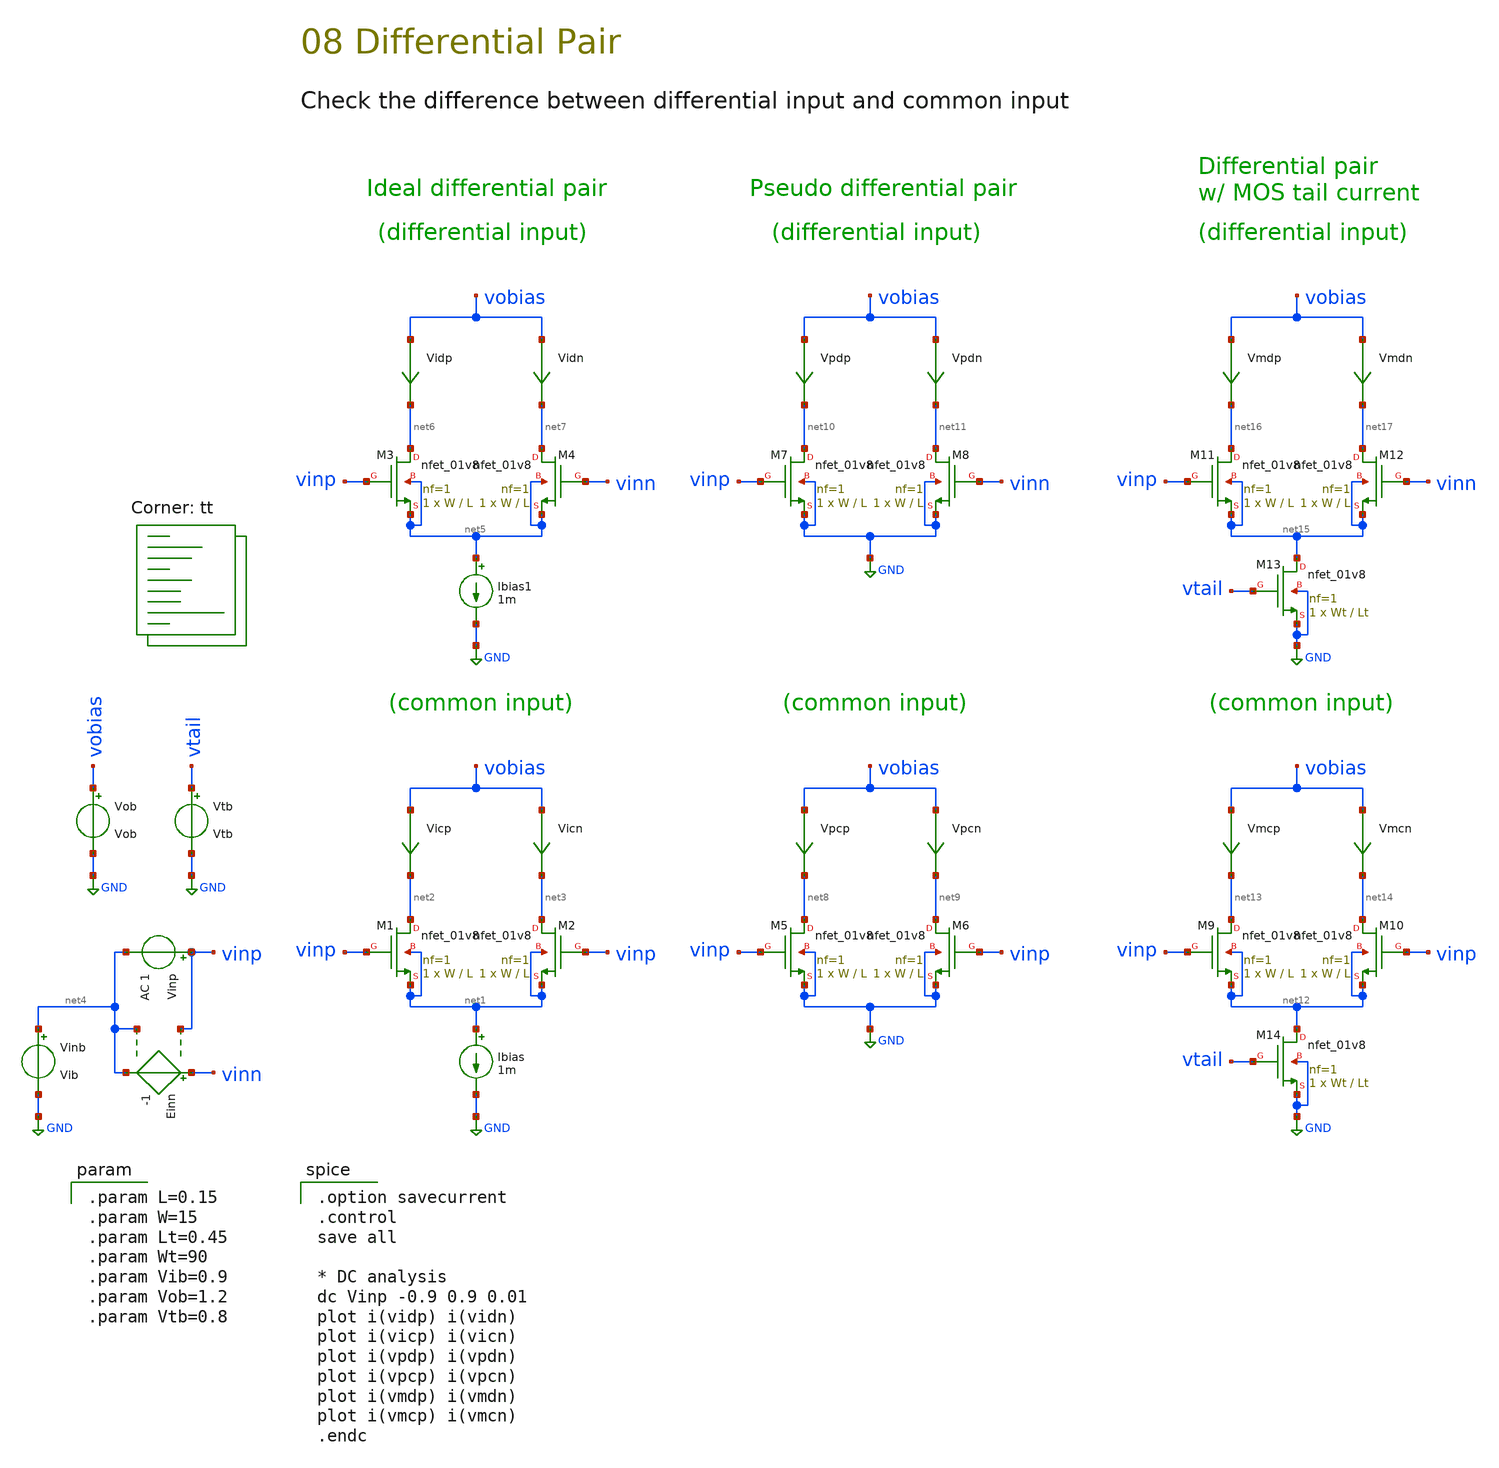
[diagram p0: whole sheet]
** sch_path: 08-a_diff-pair.sch
**.subckt 08-a_diff-pair
Vob vobias GND Vob
XM1 net2 vinp net1 net1 sky130_fd_pr__nfet_01v8 L=L W=W nf=1 ad='int((1 + 1)/2) * W / 1 * 0.29' as='int((1 + 2)/2) * W / 1 * 0.29'
+ pd='2*int((1 + 1)/2) * (W / 1 + 0.29)' ps='2*int((1 + 2)/2) * (W / 1 + 0.29)' nrd='0.29 / W ' nrs='0.29 / W '
+ sa=0 sb=0 sd=0 mult=1 m=1
Vicn vobias net3 0
.save i(vicn)
XM2 net3 vinp net1 net1 sky130_fd_pr__nfet_01v8 L=L W=W nf=1 ad='int((1 + 1)/2) * W / 1 * 0.29' as='int((1 + 2)/2) * W / 1 * 0.29'
+ pd='2*int((1 + 1)/2) * (W / 1 + 0.29)' ps='2*int((1 + 2)/2) * (W / 1 + 0.29)' nrd='0.29 / W ' nrs='0.29 / W '
+ sa=0 sb=0 sd=0 mult=1 m=1
Vinb net4 GND Vib
Vinp vinp net4 AC 1
Vicp vobias net2 0
.save i(vicp)
Ibias net1 GND 1m
Einn vinn net4 vinp net4 -1
XM3 net6 vinp net5 net5 sky130_fd_pr__nfet_01v8 L=L W=W nf=1 ad='int((1 + 1)/2) * W / 1 * 0.29' as='int((1 + 2)/2) * W / 1 * 0.29'
+ pd='2*int((1 + 1)/2) * (W / 1 + 0.29)' ps='2*int((1 + 2)/2) * (W / 1 + 0.29)' nrd='0.29 / W ' nrs='0.29 / W '
+ sa=0 sb=0 sd=0 mult=1 m=1
Vidn vobias net7 0
.save i(vidn)
XM4 net7 vinn net5 net5 sky130_fd_pr__nfet_01v8 L=L W=W nf=1 ad='int((1 + 1)/2) * W / 1 * 0.29' as='int((1 + 2)/2) * W / 1 * 0.29'
+ pd='2*int((1 + 1)/2) * (W / 1 + 0.29)' ps='2*int((1 + 2)/2) * (W / 1 + 0.29)' nrd='0.29 / W ' nrs='0.29 / W '
+ sa=0 sb=0 sd=0 mult=1 m=1
Vidp vobias net6 0
.save i(vidp)
Ibias1 net5 GND 1m
XM5 net8 vinp GND GND sky130_fd_pr__nfet_01v8 L=L W=W nf=1 ad='int((1 + 1)/2) * W / 1 * 0.29' as='int((1 + 2)/2) * W / 1 * 0.29'
+ pd='2*int((1 + 1)/2) * (W / 1 + 0.29)' ps='2*int((1 + 2)/2) * (W / 1 + 0.29)' nrd='0.29 / W ' nrs='0.29 / W '
+ sa=0 sb=0 sd=0 mult=1 m=1
Vpcn vobias net9 0
.save i(vpcn)
XM6 net9 vinp GND GND sky130_fd_pr__nfet_01v8 L=L W=W nf=1 ad='int((1 + 1)/2) * W / 1 * 0.29' as='int((1 + 2)/2) * W / 1 * 0.29'
+ pd='2*int((1 + 1)/2) * (W / 1 + 0.29)' ps='2*int((1 + 2)/2) * (W / 1 + 0.29)' nrd='0.29 / W ' nrs='0.29 / W '
+ sa=0 sb=0 sd=0 mult=1 m=1
Vpcp vobias net8 0
.save i(vpcp)
XM7 net10 vinp GND GND sky130_fd_pr__nfet_01v8 L=L W=W nf=1 ad='int((1 + 1)/2) * W / 1 * 0.29' as='int((1 + 2)/2) * W / 1 * 0.29'
+ pd='2*int((1 + 1)/2) * (W / 1 + 0.29)' ps='2*int((1 + 2)/2) * (W / 1 + 0.29)' nrd='0.29 / W ' nrs='0.29 / W '
+ sa=0 sb=0 sd=0 mult=1 m=1
Vpdn vobias net11 0
.save i(vpdn)
XM8 net11 vinn GND GND sky130_fd_pr__nfet_01v8 L=L W=W nf=1 ad='int((1 + 1)/2) * W / 1 * 0.29' as='int((1 + 2)/2) * W / 1 * 0.29'
+ pd='2*int((1 + 1)/2) * (W / 1 + 0.29)' ps='2*int((1 + 2)/2) * (W / 1 + 0.29)' nrd='0.29 / W ' nrs='0.29 / W '
+ sa=0 sb=0 sd=0 mult=1 m=1
Vpdp vobias net10 0
.save i(vpdp)
XM9 net13 vinp net12 net12 sky130_fd_pr__nfet_01v8 L=L W=W nf=1 ad='int((1 + 1)/2) * W / 1 * 0.29' as='int((1 + 2)/2) * W / 1 * 0.29'
+ pd='2*int((1 + 1)/2) * (W / 1 + 0.29)' ps='2*int((1 + 2)/2) * (W / 1 + 0.29)' nrd='0.29 / W ' nrs='0.29 / W '
+ sa=0 sb=0 sd=0 mult=1 m=1
Vmcn vobias net14 0
.save i(vmcn)
XM10 net14 vinp net12 net12 sky130_fd_pr__nfet_01v8 L=L W=W nf=1 ad='int((1 + 1)/2) * W / 1 * 0.29' as='int((1 + 2)/2) * W / 1 * 0.29'
+ pd='2*int((1 + 1)/2) * (W / 1 + 0.29)' ps='2*int((1 + 2)/2) * (W / 1 + 0.29)' nrd='0.29 / W ' nrs='0.29 / W '
+ sa=0 sb=0 sd=0 mult=1 m=1
Vmcp vobias net13 0
.save i(vmcp)
XM11 net16 vinp net15 net15 sky130_fd_pr__nfet_01v8 L=L W=W nf=1 ad='int((1 + 1)/2) * W / 1 * 0.29' as='int((1 + 2)/2) * W / 1 * 0.29'
+ pd='2*int((1 + 1)/2) * (W / 1 + 0.29)' ps='2*int((1 + 2)/2) * (W / 1 + 0.29)' nrd='0.29 / W ' nrs='0.29 / W '
+ sa=0 sb=0 sd=0 mult=1 m=1
Vmdn vobias net17 0
.save i(vmdn)
XM12 net17 vinn net15 net15 sky130_fd_pr__nfet_01v8 L=L W=W nf=1 ad='int((1 + 1)/2) * W / 1 * 0.29' as='int((1 + 2)/2) * W / 1 * 0.29'
+ pd='2*int((1 + 1)/2) * (W / 1 + 0.29)' ps='2*int((1 + 2)/2) * (W / 1 + 0.29)' nrd='0.29 / W ' nrs='0.29 / W '
+ sa=0 sb=0 sd=0 mult=1 m=1
Vmdp vobias net16 0
.save i(vmdp)
XM13 net15 vtail GND GND sky130_fd_pr__nfet_01v8 L=Lt W=Wt nf=1 ad='int((1 + 1)/2) * Wt / 1 * 0.29' as='int((1 + 2)/2) * Wt / 1 * 0.29'
+ pd='2*int((1 + 1)/2) * (Wt / 1 + 0.29)' ps='2*int((1 + 2)/2) * (Wt / 1 + 0.29)' nrd='0.29 / Wt ' nrs='0.29 / Wt '
+ sa=0 sb=0 sd=0 mult=1 m=1
Vtb vtail GND Vtb
XM14 net12 vtail GND GND sky130_fd_pr__nfet_01v8 L=Lt W=Wt nf=1 ad='int((1 + 1)/2) * Wt / 1 * 0.29' as='int((1 + 2)/2) * Wt / 1 * 0.29'
+ pd='2*int((1 + 1)/2) * (Wt / 1 + 0.29)' ps='2*int((1 + 2)/2) * (Wt / 1 + 0.29)' nrd='0.29 / Wt ' nrs='0.29 / Wt '
+ sa=0 sb=0 sd=0 mult=1 m=1
**** begin user architecture code
.lib $::SKYWATER_MODELS/sky130.lib.spice tt

.param L=0.15
.param W=15
.param Lt=0.45
.param Wt=90
.param Vib=0.9
.param Vob=1.2
.param Vtb=0.8


.option savecurrent
.control
save all

* DC analysis
dc Vinp -0.9 0.9 0.01
plot i(vidp) i(vidn)
plot i(vicp) i(vicn)
plot i(vpdp) i(vpdn)
plot i(vpcp) i(vpcn)
plot i(vmdp) i(vmdn)
plot i(vmcp) i(vmcn)
.endc

**** end user architecture code
**.ends
.GLOBAL GND
.end
